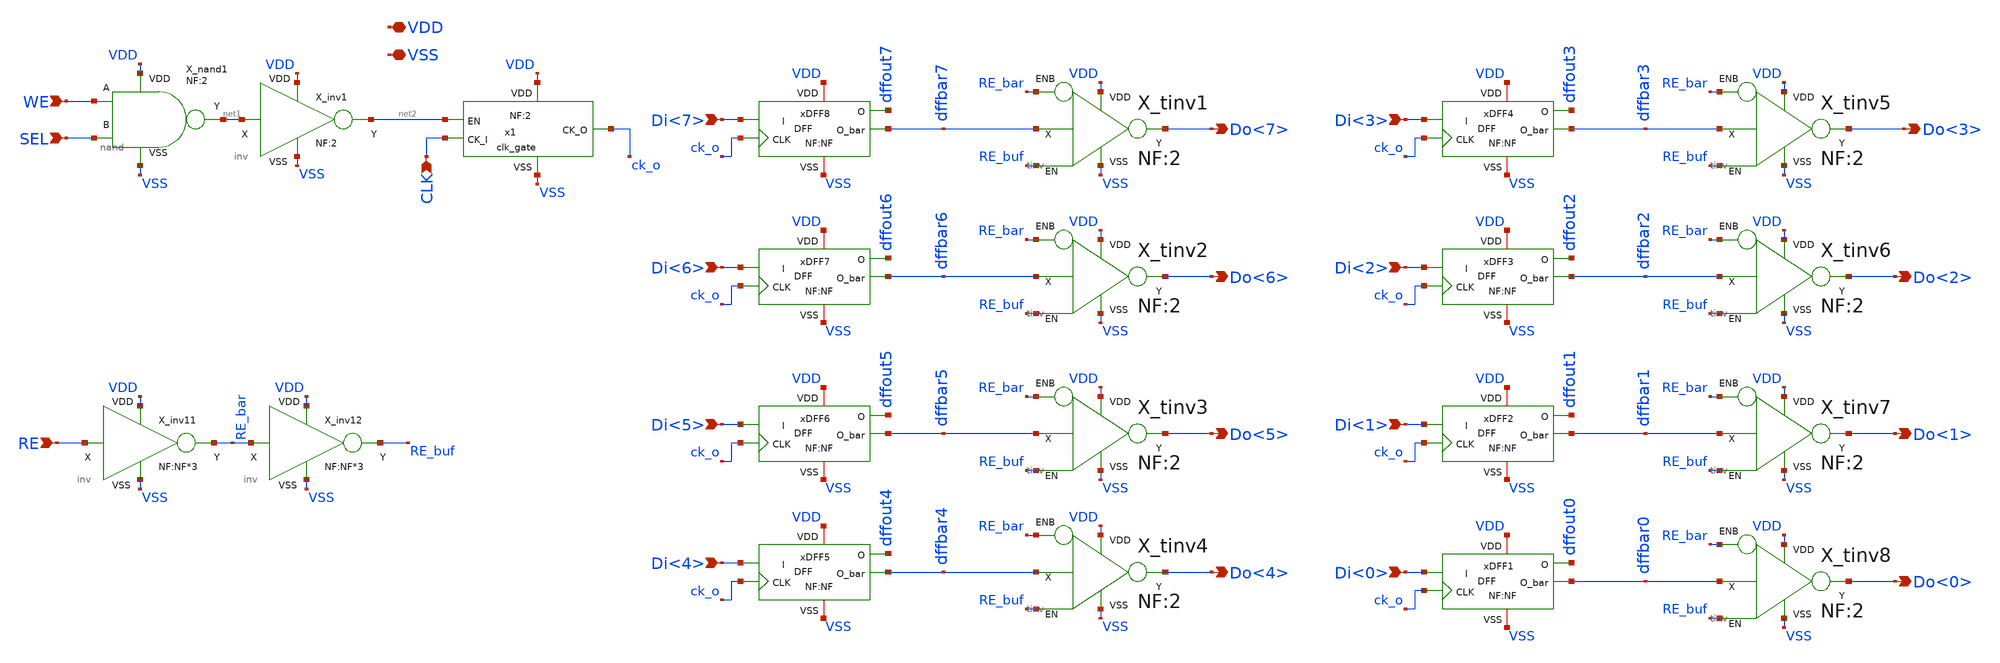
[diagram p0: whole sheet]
** sch_path: xschem_lib/DFFRAM_full_custom/byte_dff.sch
**.subckt byte_dff Do<7> Di<7> Do<6> Di<6> Do<5> Di<5> Do<4> Di<4> Do<3> Di<3> Do<2> Di<2> Do<1>
*+ Di<1> Do<0> Di<0> WE SEL CLK VDD VSS RE
*.opin Do<7>
*.ipin Di<7>
*.opin Do<6>
*.ipin Di<6>
*.opin Do<5>
*.ipin Di<5>
*.opin Do<4>
*.ipin Di<4>
*.opin Do<3>
*.ipin Di<3>
*.opin Do<2>
*.ipin Di<2>
*.opin Do<1>
*.ipin Di<1>
*.opin Do<0>
*.ipin Di<0>
*.ipin WE
*.ipin SEL
*.ipin CLK
*.iopin VDD
*.iopin VSS
*.ipin RE
X_nand1 SEL WE net1 VDD VSS nand NF=2
X_inv1 net1 VDD VSS net2 inv NF=2
x1 VDD net2 ck_o CLK VSS clk_gate NF=2
xDFF1 VDD VSS Di<0> dffbar0 ck_o dffout0 DFF NF=NF
X_tinv1 dffbar7 RE_buf RE_bar VDD VSS Do<7> tinv NF=2
X_tinv2 dffbar6 RE_buf RE_bar VDD VSS Do<6> tinv NF=2
X_tinv3 dffbar5 RE_buf RE_bar VDD VSS Do<5> tinv NF=2
X_tinv4 dffbar4 RE_buf RE_bar VDD VSS Do<4> tinv NF=2
X_tinv5 dffbar3 RE_buf RE_bar VDD VSS Do<3> tinv NF=2
X_tinv6 dffbar2 RE_buf RE_bar VDD VSS Do<2> tinv NF=2
X_tinv7 dffbar1 RE_buf RE_bar VDD VSS Do<1> tinv NF=2
X_tinv8 dffbar0 RE_buf RE_bar VDD VSS Do<0> tinv NF=2
X_inv11 RE VDD VSS RE_bar inv NF=NF*3
X_inv12 RE_bar VDD VSS RE_buf inv NF=NF*3
xDFF2 VDD VSS Di<1> dffbar1 ck_o dffout1 DFF NF=NF
xDFF3 VDD VSS Di<2> dffbar2 ck_o dffout2 DFF NF=NF
xDFF4 VDD VSS Di<3> dffbar3 ck_o dffout3 DFF NF=NF
xDFF5 VDD VSS Di<4> dffbar4 ck_o dffout4 DFF NF=NF
xDFF6 VDD VSS Di<5> dffbar5 ck_o dffout5 DFF NF=NF
xDFF7 VDD VSS Di<6> dffbar6 ck_o dffout6 DFF NF=NF
xDFF8 VDD VSS Di<7> dffbar7 ck_o dffout7 DFF NF=NF
**.ends
.end
